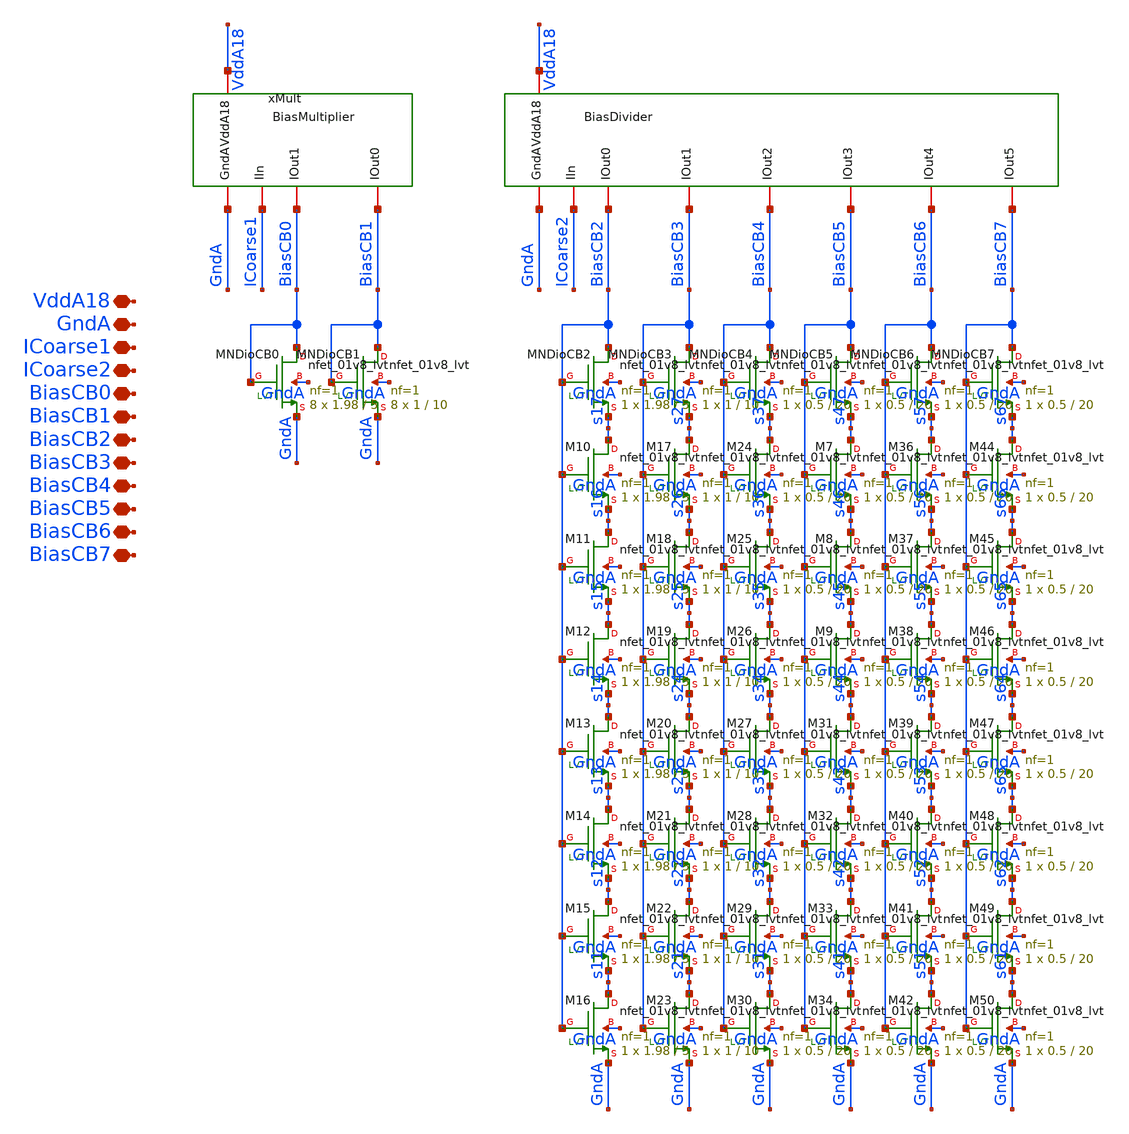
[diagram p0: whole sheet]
** sch_path: analog/xschem/BiasCoarseMBDivider.sch
**.subckt BiasCoarseMBDivider VddA18 GndA ICoarse1 BiasCB0 BiasCB1 BiasCB2 BiasCB3 BiasCB4 BiasCB5
*+ BiasCB6 BiasCB7 ICoarse2
*.iopin VddA18
*.iopin GndA
*.iopin ICoarse1
*.iopin BiasCB0
*.iopin BiasCB1
*.iopin BiasCB2
*.iopin BiasCB3
*.iopin BiasCB4
*.iopin BiasCB5
*.iopin BiasCB6
*.iopin BiasCB7
*.iopin ICoarse2
x1 GndA VddA18 ICoarse2 BiasCB2 BiasCB3 BiasCB4 BiasCB5 BiasCB6 BiasCB7 BiasDivider
xMult GndA VddA18 ICoarse1 BiasCB0 BiasCB1 BiasMultiplier
XMNDioCB0 BiasCB0 BiasCB0 GndA GndA sky130_fd_pr__nfet_01v8_lvt L=5 W=1.98 nf=1 ad='int((1 + 1)/2) * 1.98 / 1 * 0.29'
+ as='int((1 + 2)/2) * 1.98 / 1 * 0.29' pd='2*int((1 + 1)/2) * (1.98 / 1 + 0.29)' ps='2*int((1 + 2)/2) * (1.98 / 1 + 0.29)'
+ nrd='0.29 / 1.98 ' nrs='0.29 / 1.98 ' sa=0 sb=0 sd=0 mult=8 m=8
XMNDioCB1 BiasCB1 BiasCB1 GndA GndA sky130_fd_pr__nfet_01v8_lvt L=10 W=1 nf=1 ad='int((1 + 1)/2) * 1 / 1 * 0.29'
+ as='int((1 + 2)/2) * 1 / 1 * 0.29' pd='2*int((1 + 1)/2) * (1 / 1 + 0.29)' ps='2*int((1 + 2)/2) * (1 / 1 + 0.29)'
+ nrd='0.29 / 1 ' nrs='0.29 / 1 ' sa=0 sb=0 sd=0 mult=8 m=8
XMNDioCB2 BiasCB2 BiasCB2 s17 GndA sky130_fd_pr__nfet_01v8_lvt L=5 W=1.98 nf=1 ad='int((1 + 1)/2) * 1.98 / 1 * 0.29'
+ as='int((1 + 2)/2) * 1.98 / 1 * 0.29' pd='2*int((1 + 1)/2) * (1.98 / 1 + 0.29)' ps='2*int((1 + 2)/2) * (1.98 / 1 + 0.29)'
+ nrd='0.29 / 1.98 ' nrs='0.29 / 1.98 ' sa=0 sb=0 sd=0 mult=1 m=1
XMNDioCB3 BiasCB3 BiasCB3 s27 GndA sky130_fd_pr__nfet_01v8_lvt L=10 W=1 nf=1 ad='int((1 + 1)/2) * 1 / 1 * 0.29'
+ as='int((1 + 2)/2) * 1 / 1 * 0.29' pd='2*int((1 + 1)/2) * (1 / 1 + 0.29)' ps='2*int((1 + 2)/2) * (1 / 1 + 0.29)'
+ nrd='0.29 / 1 ' nrs='0.29 / 1 ' sa=0 sb=0 sd=0 mult=1 m=1
XMNDioCB4 BiasCB4 BiasCB4 s37 GndA sky130_fd_pr__nfet_01v8_lvt L=20 W=0.5 nf=1 ad='int((1 + 1)/2) * 0.5 / 1 * 0.29'
+ as='int((1 + 2)/2) * 0.5 / 1 * 0.29' pd='2*int((1 + 1)/2) * (0.5 / 1 + 0.29)' ps='2*int((1 + 2)/2) * (0.5 / 1 + 0.29)'
+ nrd='0.29 / 0.5 ' nrs='0.29 / 0.5 ' sa=0 sb=0 sd=0 mult=1 m=1
XM10 s17 BiasCB2 s16 GndA sky130_fd_pr__nfet_01v8_lvt L=5 W=1.98 nf=1 ad='int((1 + 1)/2) * 1.98 / 1 * 0.29'
+ as='int((1 + 2)/2) * 1.98 / 1 * 0.29' pd='2*int((1 + 1)/2) * (1.98 / 1 + 0.29)' ps='2*int((1 + 2)/2) * (1.98 / 1 + 0.29)'
+ nrd='0.29 / 1.98 ' nrs='0.29 / 1.98 ' sa=0 sb=0 sd=0 mult=1 m=1
XM11 s16 BiasCB2 s15 GndA sky130_fd_pr__nfet_01v8_lvt L=5 W=1.98 nf=1 ad='int((1 + 1)/2) * 1.98 / 1 * 0.29'
+ as='int((1 + 2)/2) * 1.98 / 1 * 0.29' pd='2*int((1 + 1)/2) * (1.98 / 1 + 0.29)' ps='2*int((1 + 2)/2) * (1.98 / 1 + 0.29)'
+ nrd='0.29 / 1.98 ' nrs='0.29 / 1.98 ' sa=0 sb=0 sd=0 mult=1 m=1
XM12 s15 BiasCB2 s14 GndA sky130_fd_pr__nfet_01v8_lvt L=5 W=1.98 nf=1 ad='int((1 + 1)/2) * 1.98 / 1 * 0.29'
+ as='int((1 + 2)/2) * 1.98 / 1 * 0.29' pd='2*int((1 + 1)/2) * (1.98 / 1 + 0.29)' ps='2*int((1 + 2)/2) * (1.98 / 1 + 0.29)'
+ nrd='0.29 / 1.98 ' nrs='0.29 / 1.98 ' sa=0 sb=0 sd=0 mult=1 m=1
XM13 s14 BiasCB2 s13 GndA sky130_fd_pr__nfet_01v8_lvt L=5 W=1.98 nf=1 ad='int((1 + 1)/2) * 1.98 / 1 * 0.29'
+ as='int((1 + 2)/2) * 1.98 / 1 * 0.29' pd='2*int((1 + 1)/2) * (1.98 / 1 + 0.29)' ps='2*int((1 + 2)/2) * (1.98 / 1 + 0.29)'
+ nrd='0.29 / 1.98 ' nrs='0.29 / 1.98 ' sa=0 sb=0 sd=0 mult=1 m=1
XM14 s13 BiasCB2 s12 GndA sky130_fd_pr__nfet_01v8_lvt L=5 W=1.98 nf=1 ad='int((1 + 1)/2) * 1.98 / 1 * 0.29'
+ as='int((1 + 2)/2) * 1.98 / 1 * 0.29' pd='2*int((1 + 1)/2) * (1.98 / 1 + 0.29)' ps='2*int((1 + 2)/2) * (1.98 / 1 + 0.29)'
+ nrd='0.29 / 1.98 ' nrs='0.29 / 1.98 ' sa=0 sb=0 sd=0 mult=1 m=1
XM15 s12 BiasCB2 s11 GndA sky130_fd_pr__nfet_01v8_lvt L=5 W=1.98 nf=1 ad='int((1 + 1)/2) * 1.98 / 1 * 0.29'
+ as='int((1 + 2)/2) * 1.98 / 1 * 0.29' pd='2*int((1 + 1)/2) * (1.98 / 1 + 0.29)' ps='2*int((1 + 2)/2) * (1.98 / 1 + 0.29)'
+ nrd='0.29 / 1.98 ' nrs='0.29 / 1.98 ' sa=0 sb=0 sd=0 mult=1 m=1
XM16 s11 BiasCB2 GndA GndA sky130_fd_pr__nfet_01v8_lvt L=5 W=1.98 nf=1 ad='int((1 + 1)/2) * 1.98 / 1 * 0.29'
+ as='int((1 + 2)/2) * 1.98 / 1 * 0.29' pd='2*int((1 + 1)/2) * (1.98 / 1 + 0.29)' ps='2*int((1 + 2)/2) * (1.98 / 1 + 0.29)'
+ nrd='0.29 / 1.98 ' nrs='0.29 / 1.98 ' sa=0 sb=0 sd=0 mult=1 m=1
XM17 s27 BiasCB3 s26 GndA sky130_fd_pr__nfet_01v8_lvt L=10 W=1 nf=1 ad='int((1 + 1)/2) * 1 / 1 * 0.29'
+ as='int((1 + 2)/2) * 1 / 1 * 0.29' pd='2*int((1 + 1)/2) * (1 / 1 + 0.29)' ps='2*int((1 + 2)/2) * (1 / 1 + 0.29)'
+ nrd='0.29 / 1 ' nrs='0.29 / 1 ' sa=0 sb=0 sd=0 mult=1 m=1
XM18 s26 BiasCB3 s25 GndA sky130_fd_pr__nfet_01v8_lvt L=10 W=1 nf=1 ad='int((1 + 1)/2) * 1 / 1 * 0.29'
+ as='int((1 + 2)/2) * 1 / 1 * 0.29' pd='2*int((1 + 1)/2) * (1 / 1 + 0.29)' ps='2*int((1 + 2)/2) * (1 / 1 + 0.29)'
+ nrd='0.29 / 1 ' nrs='0.29 / 1 ' sa=0 sb=0 sd=0 mult=1 m=1
XM19 s25 BiasCB3 s24 GndA sky130_fd_pr__nfet_01v8_lvt L=10 W=1 nf=1 ad='int((1 + 1)/2) * 1 / 1 * 0.29'
+ as='int((1 + 2)/2) * 1 / 1 * 0.29' pd='2*int((1 + 1)/2) * (1 / 1 + 0.29)' ps='2*int((1 + 2)/2) * (1 / 1 + 0.29)'
+ nrd='0.29 / 1 ' nrs='0.29 / 1 ' sa=0 sb=0 sd=0 mult=1 m=1
XM20 s24 BiasCB3 s23 GndA sky130_fd_pr__nfet_01v8_lvt L=10 W=1 nf=1 ad='int((1 + 1)/2) * 1 / 1 * 0.29'
+ as='int((1 + 2)/2) * 1 / 1 * 0.29' pd='2*int((1 + 1)/2) * (1 / 1 + 0.29)' ps='2*int((1 + 2)/2) * (1 / 1 + 0.29)'
+ nrd='0.29 / 1 ' nrs='0.29 / 1 ' sa=0 sb=0 sd=0 mult=1 m=1
XM21 s23 BiasCB3 s22 GndA sky130_fd_pr__nfet_01v8_lvt L=10 W=1 nf=1 ad='int((1 + 1)/2) * 1 / 1 * 0.29'
+ as='int((1 + 2)/2) * 1 / 1 * 0.29' pd='2*int((1 + 1)/2) * (1 / 1 + 0.29)' ps='2*int((1 + 2)/2) * (1 / 1 + 0.29)'
+ nrd='0.29 / 1 ' nrs='0.29 / 1 ' sa=0 sb=0 sd=0 mult=1 m=1
XM22 s22 BiasCB3 s21 GndA sky130_fd_pr__nfet_01v8_lvt L=10 W=1 nf=1 ad='int((1 + 1)/2) * 1 / 1 * 0.29'
+ as='int((1 + 2)/2) * 1 / 1 * 0.29' pd='2*int((1 + 1)/2) * (1 / 1 + 0.29)' ps='2*int((1 + 2)/2) * (1 / 1 + 0.29)'
+ nrd='0.29 / 1 ' nrs='0.29 / 1 ' sa=0 sb=0 sd=0 mult=1 m=1
XM23 s21 BiasCB3 GndA GndA sky130_fd_pr__nfet_01v8_lvt L=10 W=1 nf=1 ad='int((1 + 1)/2) * 1 / 1 * 0.29'
+ as='int((1 + 2)/2) * 1 / 1 * 0.29' pd='2*int((1 + 1)/2) * (1 / 1 + 0.29)' ps='2*int((1 + 2)/2) * (1 / 1 + 0.29)'
+ nrd='0.29 / 1 ' nrs='0.29 / 1 ' sa=0 sb=0 sd=0 mult=1 m=1
XM24 s37 BiasCB4 s36 GndA sky130_fd_pr__nfet_01v8_lvt L=20 W=0.5 nf=1 ad='int((1 + 1)/2) * 0.5 / 1 * 0.29'
+ as='int((1 + 2)/2) * 0.5 / 1 * 0.29' pd='2*int((1 + 1)/2) * (0.5 / 1 + 0.29)' ps='2*int((1 + 2)/2) * (0.5 / 1 + 0.29)'
+ nrd='0.29 / 0.5 ' nrs='0.29 / 0.5 ' sa=0 sb=0 sd=0 mult=1 m=1
XM25 s36 BiasCB4 s35 GndA sky130_fd_pr__nfet_01v8_lvt L=20 W=0.5 nf=1 ad='int((1 + 1)/2) * 0.5 / 1 * 0.29'
+ as='int((1 + 2)/2) * 0.5 / 1 * 0.29' pd='2*int((1 + 1)/2) * (0.5 / 1 + 0.29)' ps='2*int((1 + 2)/2) * (0.5 / 1 + 0.29)'
+ nrd='0.29 / 0.5 ' nrs='0.29 / 0.5 ' sa=0 sb=0 sd=0 mult=1 m=1
XM26 s35 BiasCB4 s34 GndA sky130_fd_pr__nfet_01v8_lvt L=20 W=0.5 nf=1 ad='int((1 + 1)/2) * 0.5 / 1 * 0.29'
+ as='int((1 + 2)/2) * 0.5 / 1 * 0.29' pd='2*int((1 + 1)/2) * (0.5 / 1 + 0.29)' ps='2*int((1 + 2)/2) * (0.5 / 1 + 0.29)'
+ nrd='0.29 / 0.5 ' nrs='0.29 / 0.5 ' sa=0 sb=0 sd=0 mult=1 m=1
XM27 s34 BiasCB4 s33 GndA sky130_fd_pr__nfet_01v8_lvt L=20 W=0.5 nf=1 ad='int((1 + 1)/2) * 0.5 / 1 * 0.29'
+ as='int((1 + 2)/2) * 0.5 / 1 * 0.29' pd='2*int((1 + 1)/2) * (0.5 / 1 + 0.29)' ps='2*int((1 + 2)/2) * (0.5 / 1 + 0.29)'
+ nrd='0.29 / 0.5 ' nrs='0.29 / 0.5 ' sa=0 sb=0 sd=0 mult=1 m=1
XM28 s33 BiasCB4 s32 GndA sky130_fd_pr__nfet_01v8_lvt L=20 W=0.5 nf=1 ad='int((1 + 1)/2) * 0.5 / 1 * 0.29'
+ as='int((1 + 2)/2) * 0.5 / 1 * 0.29' pd='2*int((1 + 1)/2) * (0.5 / 1 + 0.29)' ps='2*int((1 + 2)/2) * (0.5 / 1 + 0.29)'
+ nrd='0.29 / 0.5 ' nrs='0.29 / 0.5 ' sa=0 sb=0 sd=0 mult=1 m=1
XM29 s32 BiasCB4 s31 GndA sky130_fd_pr__nfet_01v8_lvt L=20 W=0.5 nf=1 ad='int((1 + 1)/2) * 0.5 / 1 * 0.29'
+ as='int((1 + 2)/2) * 0.5 / 1 * 0.29' pd='2*int((1 + 1)/2) * (0.5 / 1 + 0.29)' ps='2*int((1 + 2)/2) * (0.5 / 1 + 0.29)'
+ nrd='0.29 / 0.5 ' nrs='0.29 / 0.5 ' sa=0 sb=0 sd=0 mult=1 m=1
XM30 s31 BiasCB4 GndA GndA sky130_fd_pr__nfet_01v8_lvt L=20 W=0.5 nf=1 ad='int((1 + 1)/2) * 0.5 / 1 * 0.29'
+ as='int((1 + 2)/2) * 0.5 / 1 * 0.29' pd='2*int((1 + 1)/2) * (0.5 / 1 + 0.29)' ps='2*int((1 + 2)/2) * (0.5 / 1 + 0.29)'
+ nrd='0.29 / 0.5 ' nrs='0.29 / 0.5 ' sa=0 sb=0 sd=0 mult=1 m=1
XMNDioCB5 BiasCB5 BiasCB5 s47 GndA sky130_fd_pr__nfet_01v8_lvt L=20 W=0.5 nf=1 ad='int((1 + 1)/2) * 0.5 / 1 * 0.29'
+ as='int((1 + 2)/2) * 0.5 / 1 * 0.29' pd='2*int((1 + 1)/2) * (0.5 / 1 + 0.29)' ps='2*int((1 + 2)/2) * (0.5 / 1 + 0.29)'
+ nrd='0.29 / 0.5 ' nrs='0.29 / 0.5 ' sa=0 sb=0 sd=0 mult=1 m=1
XM7 s47 BiasCB5 s46 GndA sky130_fd_pr__nfet_01v8_lvt L=20 W=0.5 nf=1 ad='int((1 + 1)/2) * 0.5 / 1 * 0.29'
+ as='int((1 + 2)/2) * 0.5 / 1 * 0.29' pd='2*int((1 + 1)/2) * (0.5 / 1 + 0.29)' ps='2*int((1 + 2)/2) * (0.5 / 1 + 0.29)'
+ nrd='0.29 / 0.5 ' nrs='0.29 / 0.5 ' sa=0 sb=0 sd=0 mult=1 m=1
XM8 s46 BiasCB5 s45 GndA sky130_fd_pr__nfet_01v8_lvt L=20 W=0.5 nf=1 ad='int((1 + 1)/2) * 0.5 / 1 * 0.29'
+ as='int((1 + 2)/2) * 0.5 / 1 * 0.29' pd='2*int((1 + 1)/2) * (0.5 / 1 + 0.29)' ps='2*int((1 + 2)/2) * (0.5 / 1 + 0.29)'
+ nrd='0.29 / 0.5 ' nrs='0.29 / 0.5 ' sa=0 sb=0 sd=0 mult=1 m=1
XM9 s45 BiasCB5 s44 GndA sky130_fd_pr__nfet_01v8_lvt L=20 W=0.5 nf=1 ad='int((1 + 1)/2) * 0.5 / 1 * 0.29'
+ as='int((1 + 2)/2) * 0.5 / 1 * 0.29' pd='2*int((1 + 1)/2) * (0.5 / 1 + 0.29)' ps='2*int((1 + 2)/2) * (0.5 / 1 + 0.29)'
+ nrd='0.29 / 0.5 ' nrs='0.29 / 0.5 ' sa=0 sb=0 sd=0 mult=1 m=1
XM31 s44 BiasCB5 s43 GndA sky130_fd_pr__nfet_01v8_lvt L=20 W=0.5 nf=1 ad='int((1 + 1)/2) * 0.5 / 1 * 0.29'
+ as='int((1 + 2)/2) * 0.5 / 1 * 0.29' pd='2*int((1 + 1)/2) * (0.5 / 1 + 0.29)' ps='2*int((1 + 2)/2) * (0.5 / 1 + 0.29)'
+ nrd='0.29 / 0.5 ' nrs='0.29 / 0.5 ' sa=0 sb=0 sd=0 mult=1 m=1
XM32 s43 BiasCB5 s42 GndA sky130_fd_pr__nfet_01v8_lvt L=20 W=0.5 nf=1 ad='int((1 + 1)/2) * 0.5 / 1 * 0.29'
+ as='int((1 + 2)/2) * 0.5 / 1 * 0.29' pd='2*int((1 + 1)/2) * (0.5 / 1 + 0.29)' ps='2*int((1 + 2)/2) * (0.5 / 1 + 0.29)'
+ nrd='0.29 / 0.5 ' nrs='0.29 / 0.5 ' sa=0 sb=0 sd=0 mult=1 m=1
XM33 s42 BiasCB5 s41 GndA sky130_fd_pr__nfet_01v8_lvt L=20 W=0.5 nf=1 ad='int((1 + 1)/2) * 0.5 / 1 * 0.29'
+ as='int((1 + 2)/2) * 0.5 / 1 * 0.29' pd='2*int((1 + 1)/2) * (0.5 / 1 + 0.29)' ps='2*int((1 + 2)/2) * (0.5 / 1 + 0.29)'
+ nrd='0.29 / 0.5 ' nrs='0.29 / 0.5 ' sa=0 sb=0 sd=0 mult=1 m=1
XM34 s41 BiasCB5 GndA GndA sky130_fd_pr__nfet_01v8_lvt L=20 W=0.5 nf=1 ad='int((1 + 1)/2) * 0.5 / 1 * 0.29'
+ as='int((1 + 2)/2) * 0.5 / 1 * 0.29' pd='2*int((1 + 1)/2) * (0.5 / 1 + 0.29)' ps='2*int((1 + 2)/2) * (0.5 / 1 + 0.29)'
+ nrd='0.29 / 0.5 ' nrs='0.29 / 0.5 ' sa=0 sb=0 sd=0 mult=1 m=1
XMNDioCB6 BiasCB6 BiasCB6 s57 GndA sky130_fd_pr__nfet_01v8_lvt L=20 W=0.5 nf=1 ad='int((1 + 1)/2) * 0.5 / 1 * 0.29'
+ as='int((1 + 2)/2) * 0.5 / 1 * 0.29' pd='2*int((1 + 1)/2) * (0.5 / 1 + 0.29)' ps='2*int((1 + 2)/2) * (0.5 / 1 + 0.29)'
+ nrd='0.29 / 0.5 ' nrs='0.29 / 0.5 ' sa=0 sb=0 sd=0 mult=1 m=1
XM36 s57 BiasCB6 s56 GndA sky130_fd_pr__nfet_01v8_lvt L=20 W=0.5 nf=1 ad='int((1 + 1)/2) * 0.5 / 1 * 0.29'
+ as='int((1 + 2)/2) * 0.5 / 1 * 0.29' pd='2*int((1 + 1)/2) * (0.5 / 1 + 0.29)' ps='2*int((1 + 2)/2) * (0.5 / 1 + 0.29)'
+ nrd='0.29 / 0.5 ' nrs='0.29 / 0.5 ' sa=0 sb=0 sd=0 mult=1 m=1
XM37 s56 BiasCB6 s55 GndA sky130_fd_pr__nfet_01v8_lvt L=20 W=0.5 nf=1 ad='int((1 + 1)/2) * 0.5 / 1 * 0.29'
+ as='int((1 + 2)/2) * 0.5 / 1 * 0.29' pd='2*int((1 + 1)/2) * (0.5 / 1 + 0.29)' ps='2*int((1 + 2)/2) * (0.5 / 1 + 0.29)'
+ nrd='0.29 / 0.5 ' nrs='0.29 / 0.5 ' sa=0 sb=0 sd=0 mult=1 m=1
XM38 s55 BiasCB6 s54 GndA sky130_fd_pr__nfet_01v8_lvt L=20 W=0.5 nf=1 ad='int((1 + 1)/2) * 0.5 / 1 * 0.29'
+ as='int((1 + 2)/2) * 0.5 / 1 * 0.29' pd='2*int((1 + 1)/2) * (0.5 / 1 + 0.29)' ps='2*int((1 + 2)/2) * (0.5 / 1 + 0.29)'
+ nrd='0.29 / 0.5 ' nrs='0.29 / 0.5 ' sa=0 sb=0 sd=0 mult=1 m=1
XM39 s54 BiasCB6 s53 GndA sky130_fd_pr__nfet_01v8_lvt L=20 W=0.5 nf=1 ad='int((1 + 1)/2) * 0.5 / 1 * 0.29'
+ as='int((1 + 2)/2) * 0.5 / 1 * 0.29' pd='2*int((1 + 1)/2) * (0.5 / 1 + 0.29)' ps='2*int((1 + 2)/2) * (0.5 / 1 + 0.29)'
+ nrd='0.29 / 0.5 ' nrs='0.29 / 0.5 ' sa=0 sb=0 sd=0 mult=1 m=1
XM40 s53 BiasCB6 s52 GndA sky130_fd_pr__nfet_01v8_lvt L=20 W=0.5 nf=1 ad='int((1 + 1)/2) * 0.5 / 1 * 0.29'
+ as='int((1 + 2)/2) * 0.5 / 1 * 0.29' pd='2*int((1 + 1)/2) * (0.5 / 1 + 0.29)' ps='2*int((1 + 2)/2) * (0.5 / 1 + 0.29)'
+ nrd='0.29 / 0.5 ' nrs='0.29 / 0.5 ' sa=0 sb=0 sd=0 mult=1 m=1
XM41 s52 BiasCB6 s51 GndA sky130_fd_pr__nfet_01v8_lvt L=20 W=0.5 nf=1 ad='int((1 + 1)/2) * 0.5 / 1 * 0.29'
+ as='int((1 + 2)/2) * 0.5 / 1 * 0.29' pd='2*int((1 + 1)/2) * (0.5 / 1 + 0.29)' ps='2*int((1 + 2)/2) * (0.5 / 1 + 0.29)'
+ nrd='0.29 / 0.5 ' nrs='0.29 / 0.5 ' sa=0 sb=0 sd=0 mult=1 m=1
XM42 s51 BiasCB6 GndA GndA sky130_fd_pr__nfet_01v8_lvt L=20 W=0.5 nf=1 ad='int((1 + 1)/2) * 0.5 / 1 * 0.29'
+ as='int((1 + 2)/2) * 0.5 / 1 * 0.29' pd='2*int((1 + 1)/2) * (0.5 / 1 + 0.29)' ps='2*int((1 + 2)/2) * (0.5 / 1 + 0.29)'
+ nrd='0.29 / 0.5 ' nrs='0.29 / 0.5 ' sa=0 sb=0 sd=0 mult=1 m=1
XMNDioCB7 BiasCB7 BiasCB7 s67 GndA sky130_fd_pr__nfet_01v8_lvt L=20 W=0.5 nf=1 ad='int((1 + 1)/2) * 0.5 / 1 * 0.29'
+ as='int((1 + 2)/2) * 0.5 / 1 * 0.29' pd='2*int((1 + 1)/2) * (0.5 / 1 + 0.29)' ps='2*int((1 + 2)/2) * (0.5 / 1 + 0.29)'
+ nrd='0.29 / 0.5 ' nrs='0.29 / 0.5 ' sa=0 sb=0 sd=0 mult=1 m=1
XM44 s67 BiasCB7 s66 GndA sky130_fd_pr__nfet_01v8_lvt L=20 W=0.5 nf=1 ad='int((1 + 1)/2) * 0.5 / 1 * 0.29'
+ as='int((1 + 2)/2) * 0.5 / 1 * 0.29' pd='2*int((1 + 1)/2) * (0.5 / 1 + 0.29)' ps='2*int((1 + 2)/2) * (0.5 / 1 + 0.29)'
+ nrd='0.29 / 0.5 ' nrs='0.29 / 0.5 ' sa=0 sb=0 sd=0 mult=1 m=1
XM45 s66 BiasCB7 s65 GndA sky130_fd_pr__nfet_01v8_lvt L=20 W=0.5 nf=1 ad='int((1 + 1)/2) * 0.5 / 1 * 0.29'
+ as='int((1 + 2)/2) * 0.5 / 1 * 0.29' pd='2*int((1 + 1)/2) * (0.5 / 1 + 0.29)' ps='2*int((1 + 2)/2) * (0.5 / 1 + 0.29)'
+ nrd='0.29 / 0.5 ' nrs='0.29 / 0.5 ' sa=0 sb=0 sd=0 mult=1 m=1
XM46 s65 BiasCB7 s64 GndA sky130_fd_pr__nfet_01v8_lvt L=20 W=0.5 nf=1 ad='int((1 + 1)/2) * 0.5 / 1 * 0.29'
+ as='int((1 + 2)/2) * 0.5 / 1 * 0.29' pd='2*int((1 + 1)/2) * (0.5 / 1 + 0.29)' ps='2*int((1 + 2)/2) * (0.5 / 1 + 0.29)'
+ nrd='0.29 / 0.5 ' nrs='0.29 / 0.5 ' sa=0 sb=0 sd=0 mult=1 m=1
XM47 s64 BiasCB7 s63 GndA sky130_fd_pr__nfet_01v8_lvt L=20 W=0.5 nf=1 ad='int((1 + 1)/2) * 0.5 / 1 * 0.29'
+ as='int((1 + 2)/2) * 0.5 / 1 * 0.29' pd='2*int((1 + 1)/2) * (0.5 / 1 + 0.29)' ps='2*int((1 + 2)/2) * (0.5 / 1 + 0.29)'
+ nrd='0.29 / 0.5 ' nrs='0.29 / 0.5 ' sa=0 sb=0 sd=0 mult=1 m=1
XM48 s63 BiasCB7 s62 GndA sky130_fd_pr__nfet_01v8_lvt L=20 W=0.5 nf=1 ad='int((1 + 1)/2) * 0.5 / 1 * 0.29'
+ as='int((1 + 2)/2) * 0.5 / 1 * 0.29' pd='2*int((1 + 1)/2) * (0.5 / 1 + 0.29)' ps='2*int((1 + 2)/2) * (0.5 / 1 + 0.29)'
+ nrd='0.29 / 0.5 ' nrs='0.29 / 0.5 ' sa=0 sb=0 sd=0 mult=1 m=1
XM49 s62 BiasCB7 s61 GndA sky130_fd_pr__nfet_01v8_lvt L=20 W=0.5 nf=1 ad='int((1 + 1)/2) * 0.5 / 1 * 0.29'
+ as='int((1 + 2)/2) * 0.5 / 1 * 0.29' pd='2*int((1 + 1)/2) * (0.5 / 1 + 0.29)' ps='2*int((1 + 2)/2) * (0.5 / 1 + 0.29)'
+ nrd='0.29 / 0.5 ' nrs='0.29 / 0.5 ' sa=0 sb=0 sd=0 mult=1 m=1
XM50 s61 BiasCB7 GndA GndA sky130_fd_pr__nfet_01v8_lvt L=20 W=0.5 nf=1 ad='int((1 + 1)/2) * 0.5 / 1 * 0.29'
+ as='int((1 + 2)/2) * 0.5 / 1 * 0.29' pd='2*int((1 + 1)/2) * (0.5 / 1 + 0.29)' ps='2*int((1 + 2)/2) * (0.5 / 1 + 0.29)'
+ nrd='0.29 / 0.5 ' nrs='0.29 / 0.5 ' sa=0 sb=0 sd=0 mult=1 m=1
**.ends
.end
